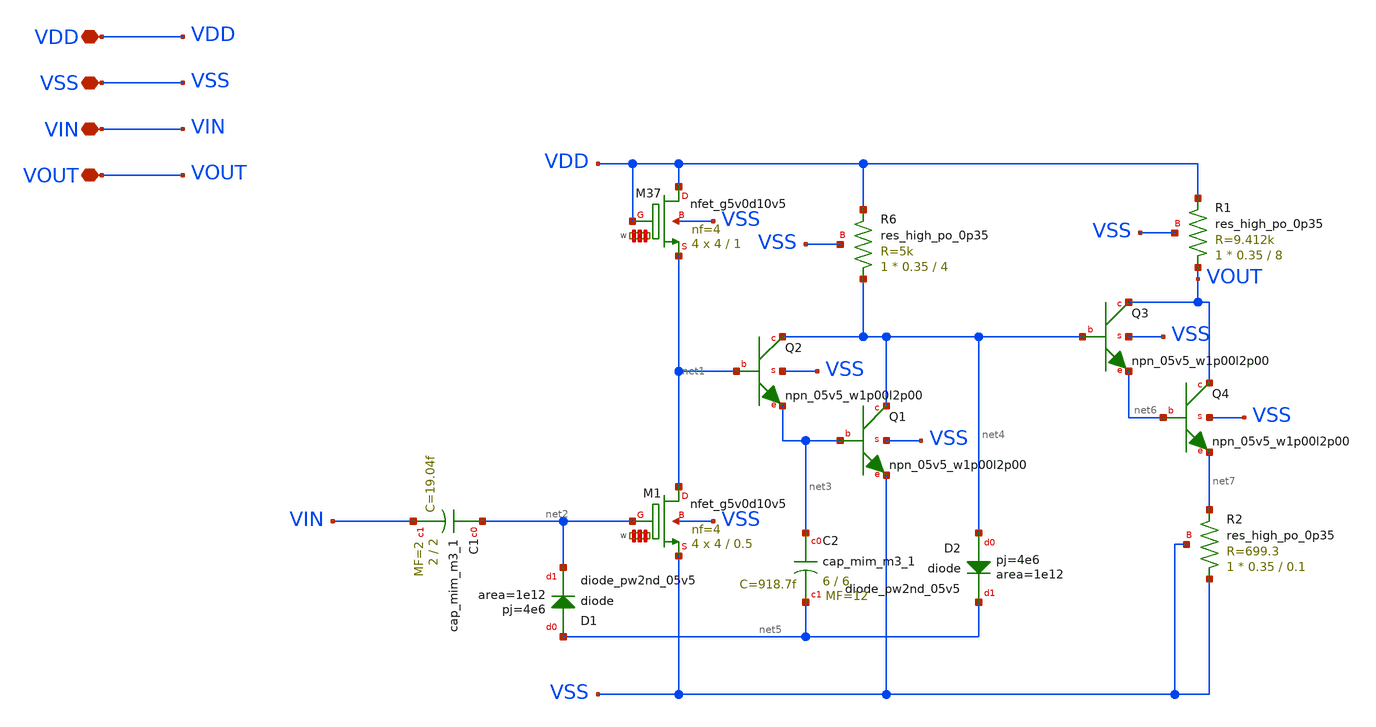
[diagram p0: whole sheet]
** sch_path: my_ip/LIB/primordial_bicmos/audio003_5V_sky130A.sch
**.subckt audio003_5V_sky130A VDD VSS VIN VOUT
*.iopin VDD
*.iopin VSS
*.iopin VIN
*.iopin VOUT
XC1 net2 VIN sky130_fd_pr__cap_mim_m3_1 W=2 L=2 MF=2 m=2
XQ2 net4 net1 net3 VSS sky130_fd_pr__npn_05v5_w1p00l2p00
XQ1 net4 net3 VSS VSS sky130_fd_pr__npn_05v5_w1p00l2p00
XR6 net4 VDD VSS sky130_fd_pr__res_high_po_0p35 L=4 mult=1 m=1
XD1 net5 net2 sky130_fd_pr__diode_pw2nd_05v5 area=1e12 pj=4e6
XD2 net4 net5 sky130_fd_pr__diode_pw2nd_05v5 area=1e12 pj=4e6
XC2 net3 net5 sky130_fd_pr__cap_mim_m3_1 W=6 L=6 MF=12 m=12
XQ3 VOUT net4 net6 VSS sky130_fd_pr__npn_05v5_w1p00l2p00
XQ4 VOUT net6 net7 VSS sky130_fd_pr__npn_05v5_w1p00l2p00
XR1 VOUT VDD VSS sky130_fd_pr__res_high_po_0p35 L=8 mult=1 m=1
XR2 VSS net7 VSS sky130_fd_pr__res_high_po_0p35 L=0.1 mult=1 m=1
XM37 VDD VDD net1 VSS sky130_fd_pr__nfet_g5v0d10v5 L=1 W='4 * 4 ' nf=4 ad='int((nf+1)/2) * W / nf * 0.29'
+ as='int((nf+2)/2) * W / nf * 0.29' pd='2*int((nf+1)/2) * (W / nf + 0.29)' ps='2*int((nf+2)/2) * (W / nf + 0.29)'
+ nrd='0.29 / W ' nrs='0.29 / W ' sa=0 sb=0 sd=0 mult=4 m=4
XM1 net1 net2 VSS VSS sky130_fd_pr__nfet_g5v0d10v5 L=0.5 W='4 * 4 ' nf=4 ad='int((nf+1)/2) * W / nf * 0.29'
+ as='int((nf+2)/2) * W / nf * 0.29' pd='2*int((nf+1)/2) * (W / nf + 0.29)' ps='2*int((nf+2)/2) * (W / nf + 0.29)'
+ nrd='0.29 / W ' nrs='0.29 / W ' sa=0 sb=0 sd=0 mult=4 m=4
**.ends
.end
